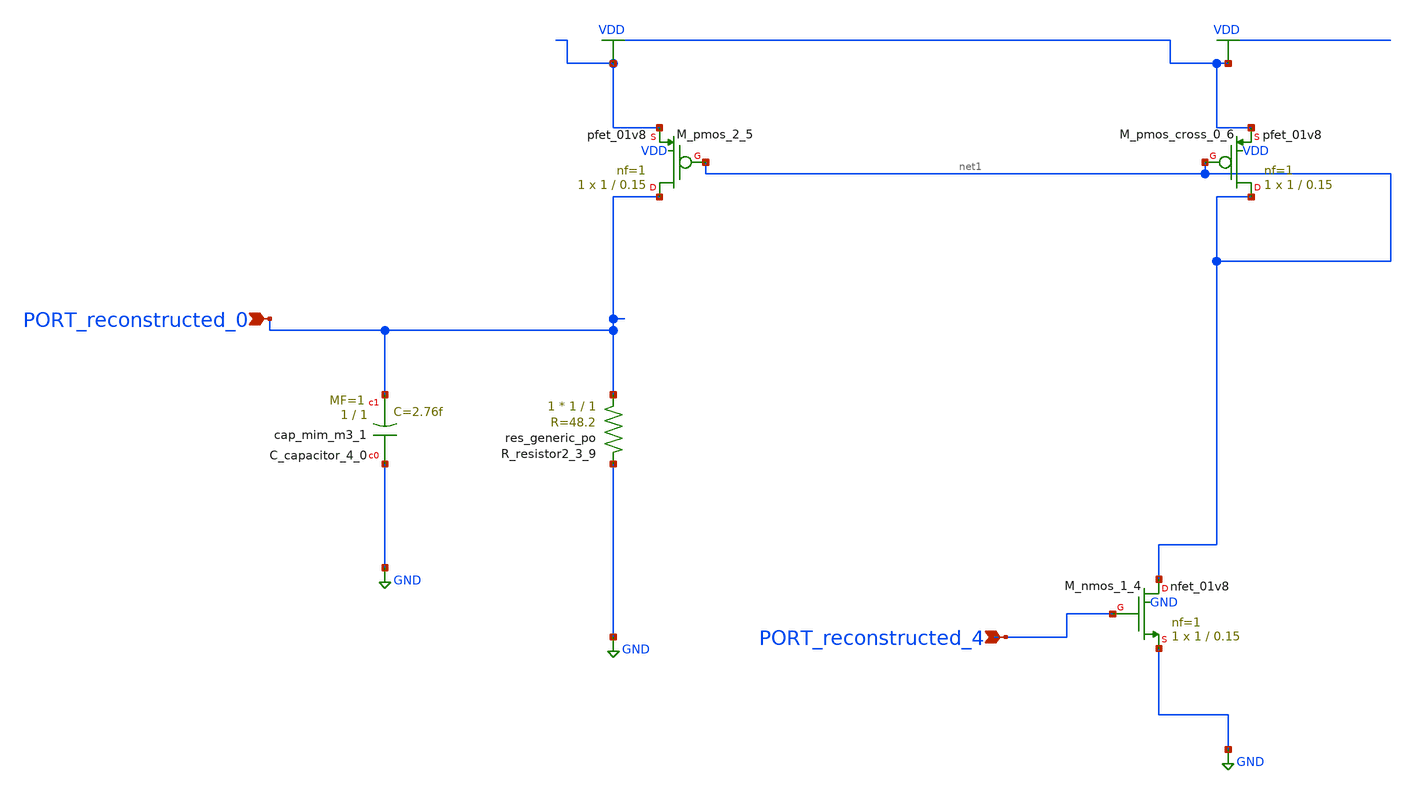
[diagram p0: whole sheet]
** sch_path: schematics/AMSNet/393.sch
**.subckt 393 PORT_reconstructed_4 PORT_reconstructed_0
*.ipin PORT_reconstructed_4
*.ipin PORT_reconstructed_0
XC_capacitor_4_0 GND PORT_reconstructed_0 sky130_fd_pr__cap_mim_m3_1 W=1 L=1 MF=1 m=1
XM_nmos_1_4 net1 PORT_reconstructed_4 GND GND sky130_fd_pr__nfet_01v8 L=0.15 W=1 nf=1 ad='int((1 + 1)/2) * 1 / 1 * 0.29'
+ as='int((1 + 2)/2) * 1 / 1 * 0.29' pd='2*int((1 + 1)/2) * (1 / 1 + 0.29)' ps='2*int((1 + 2)/2) * (1 / 1 + 0.29)'
+ nrd='0.29 / 1 ' nrs='0.29 / 1 ' sa=0 sb=0 sd=0 mult=1 m=1
XM_pmos_2_5 PORT_reconstructed_0 net1 VDD VDD sky130_fd_pr__pfet_01v8 L=0.15 W=1 nf=1 ad='int((1 + 1)/2) * 1 / 1 * 0.29'
+ as='int((1 + 2)/2) * 1 / 1 * 0.29' pd='2*int((1 + 1)/2) * (1 / 1 + 0.29)' ps='2*int((1 + 2)/2) * (1 / 1 + 0.29)'
+ nrd='0.29 / 1 ' nrs='0.29 / 1 ' sa=0 sb=0 sd=0 mult=1 m=1
XM_pmos_cross_0_6 net1 net1 VDD VDD sky130_fd_pr__pfet_01v8 L=0.15 W=1 nf=1 ad='int((1 + 1)/2) * 1 / 1 * 0.29'
+ as='int((1 + 2)/2) * 1 / 1 * 0.29' pd='2*int((1 + 1)/2) * (1 / 1 + 0.29)' ps='2*int((1 + 2)/2) * (1 / 1 + 0.29)'
+ nrd='0.29 / 1 ' nrs='0.29 / 1 ' sa=0 sb=0 sd=0 mult=1 m=1
XR_resistor2_3_9 PORT_reconstructed_0 GND sky130_fd_pr__res_generic_po W=1 L=1 m=1
**.ends
.GLOBAL GND
.GLOBAL VDD
.end
